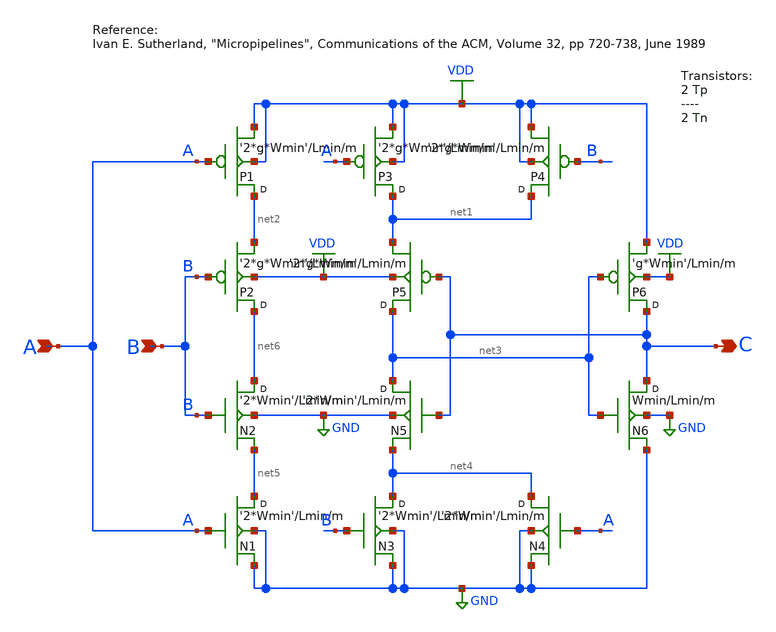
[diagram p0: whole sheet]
** sch_path: Sources/schematics/sutherland1989.sch
**.subckt sutherland1989 B C A
*.ipin B
*.opin C
*.ipin A
N2 net6 B net5 GND nmos w='2*Wmin' l=Lmin m=m
P1 net2 A VDD VDD pmos w='2*g*Wmin' l=Lmin m=m
P2 net6 B net2 VDD pmos w='2*g*Wmin' l=Lmin m=m
P3 net1 A VDD VDD pmos w='2*g*Wmin' l=Lmin m=m
P4 net1 B VDD VDD pmos w='2*g*Wmin' l=Lmin m=m
P5 net3 C net1 VDD pmos w='2*g*Wmin' l=Lmin m=m
P6 C net3 VDD VDD pmos w='g*Wmin' l=Lmin m=m
N5 net3 C net4 GND nmos w='2*Wmin' l=Lmin m=m
N1 net5 A GND GND nmos w='2*Wmin' l=Lmin m=m
N3 net4 B GND GND nmos w='2*Wmin' l=Lmin m=m
N4 net4 A GND GND nmos w='2*Wmin' l=Lmin m=m
N6 C net3 GND GND nmos w=Wmin l=Lmin m=m
**.ends
.GLOBAL GND
.GLOBAL VDD
.end
